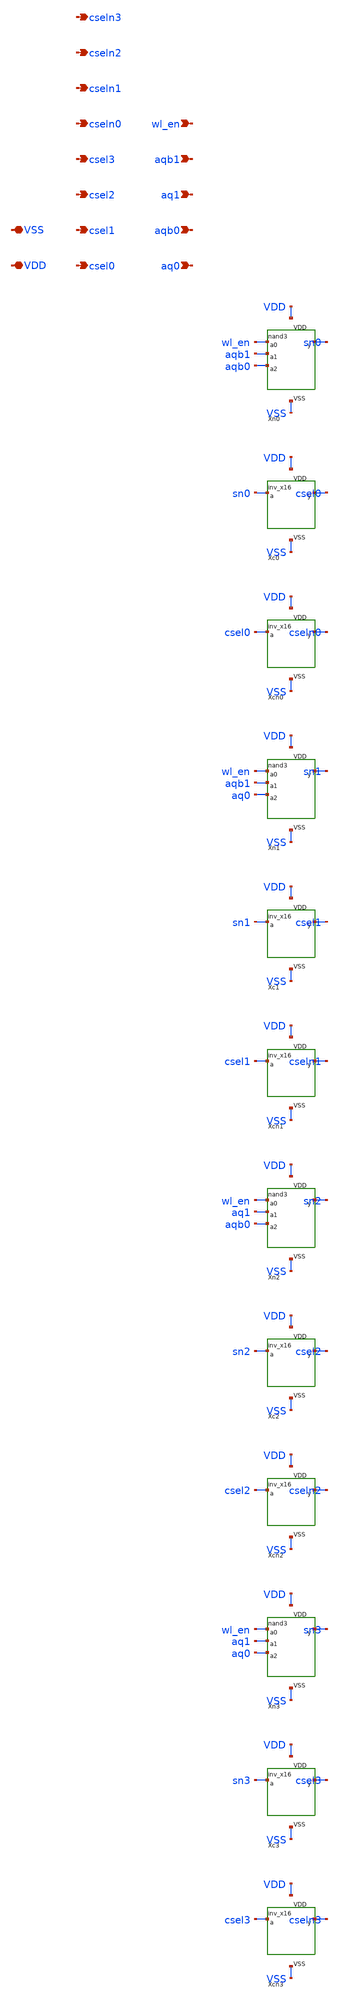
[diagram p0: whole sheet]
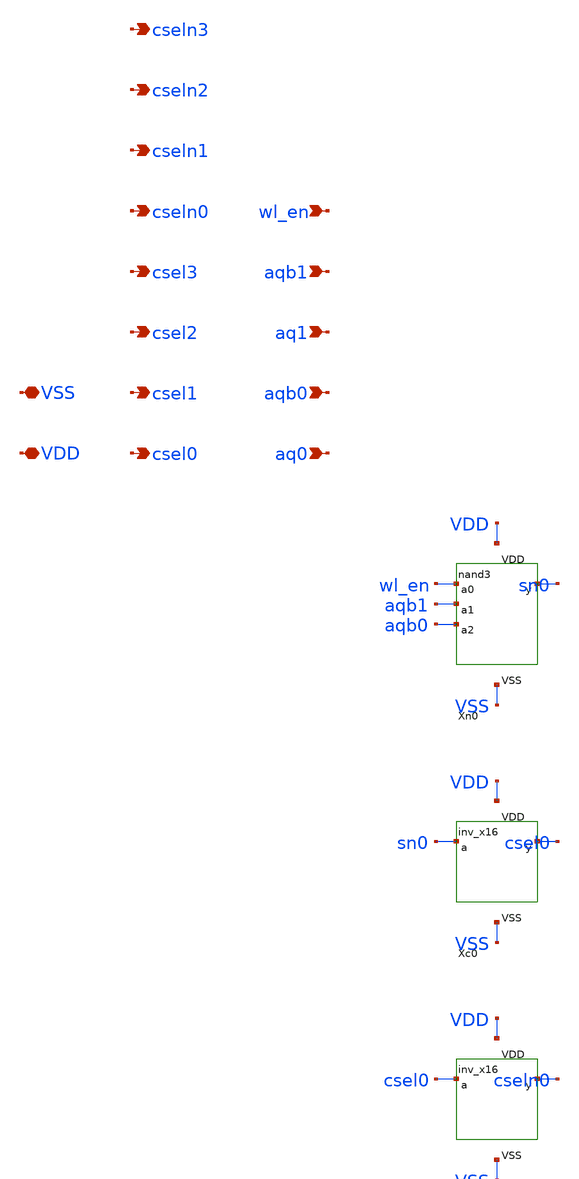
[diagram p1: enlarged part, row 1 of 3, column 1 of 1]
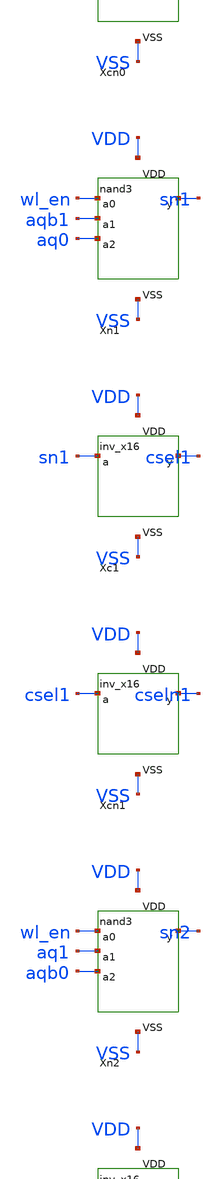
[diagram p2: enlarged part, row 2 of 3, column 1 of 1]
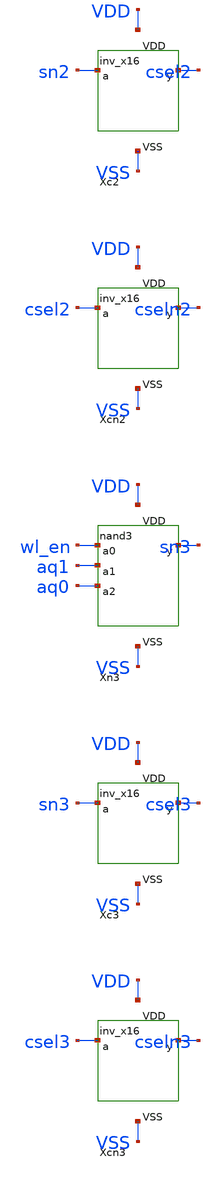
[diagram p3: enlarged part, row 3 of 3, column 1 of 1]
** sch_path: design/col_decode.sch
**.subckt col_decode aq0 aqb0 aq1 aqb1 wl_en csel0 csel1 csel2 csel3 cseln0 cseln1 cseln2 cseln3 VDD
*+ VSS
*.ipin aq0
*.ipin aqb0
*.ipin aq1
*.ipin aqb1
*.ipin wl_en
*.opin csel0
*.opin csel1
*.opin csel2
*.opin csel3
*.opin cseln0
*.opin cseln1
*.opin cseln2
*.opin cseln3
*.iopin VDD
*.iopin VSS
XXn0 wl_en aqb1 aqb0 sn0 VDD VSS nand3
XXc0 sn0 csel0 VDD VSS inv_x16
XXcn0 csel0 cseln0 VDD VSS inv_x16
XXn1 wl_en aqb1 aq0 sn1 VDD VSS nand3
XXc1 sn1 csel1 VDD VSS inv_x16
XXcn1 csel1 cseln1 VDD VSS inv_x16
XXn2 wl_en aq1 aqb0 sn2 VDD VSS nand3
XXc2 sn2 csel2 VDD VSS inv_x16
XXcn2 csel2 cseln2 VDD VSS inv_x16
XXn3 wl_en aq1 aq0 sn3 VDD VSS nand3
XXc3 sn3 csel3 VDD VSS inv_x16
XXcn3 csel3 cseln3 VDD VSS inv_x16
**.ends

* expanding   symbol:  nand3.sym # of pins=6
** sym_path: design/nand3.sym
** sch_path: design/nand3.sch
.subckt nand3 a0 a1 a2 y VDD VSS

*.ipin a0
*.ipin a1
*.ipin a2
*.opin y
*.iopin VDD
*.iopin VSS
XMP0 y a0 VDD VDD pfet_03v3 L=0.28u W=1u nf=1 ad='int((nf+1)/2) * W/nf * 0.18u' as='int((nf+2)/2) * W/nf * 0.18u'
+ pd='2*int((nf+1)/2) * (W/nf + 0.18u)' ps='2*int((nf+2)/2) * (W/nf + 0.18u)' nrd='0.18u / W' nrs='0.18u / W'
+ sa=0 sb=0 sd=0 m=1
XMP1 y a1 VDD VDD pfet_03v3 L=0.28u W=1u nf=1 ad='int((nf+1)/2) * W/nf * 0.18u' as='int((nf+2)/2) * W/nf * 0.18u'
+ pd='2*int((nf+1)/2) * (W/nf + 0.18u)' ps='2*int((nf+2)/2) * (W/nf + 0.18u)' nrd='0.18u / W' nrs='0.18u / W'
+ sa=0 sb=0 sd=0 m=1
XMP2 y a2 VDD VDD pfet_03v3 L=0.28u W=1u nf=1 ad='int((nf+1)/2) * W/nf * 0.18u' as='int((nf+2)/2) * W/nf * 0.18u'
+ pd='2*int((nf+1)/2) * (W/nf + 0.18u)' ps='2*int((nf+2)/2) * (W/nf + 0.18u)' nrd='0.18u / W' nrs='0.18u / W'
+ sa=0 sb=0 sd=0 m=1
XMN0 y a0 s1 VSS nfet_03v3 L=0.28u W=1.5u nf=1 ad='int((nf+1)/2) * W/nf * 0.18u' as='int((nf+2)/2) * W/nf * 0.18u'
+ pd='2*int((nf+1)/2) * (W/nf + 0.18u)' ps='2*int((nf+2)/2) * (W/nf + 0.18u)' nrd='0.18u / W' nrs='0.18u / W'
+ sa=0 sb=0 sd=0 m=1
XMN1 s1 a1 s2 VSS nfet_03v3 L=0.28u W=1.5u nf=1 ad='int((nf+1)/2) * W/nf * 0.18u' as='int((nf+2)/2) * W/nf * 0.18u'
+ pd='2*int((nf+1)/2) * (W/nf + 0.18u)' ps='2*int((nf+2)/2) * (W/nf + 0.18u)' nrd='0.18u / W' nrs='0.18u / W'
+ sa=0 sb=0 sd=0 m=1
XMN2 s2 a2 VSS VSS nfet_03v3 L=0.28u W=1.5u nf=1 ad='int((nf+1)/2) * W/nf * 0.18u' as='int((nf+2)/2) * W/nf * 0.18u'
+ pd='2*int((nf+1)/2) * (W/nf + 0.18u)' ps='2*int((nf+2)/2) * (W/nf + 0.18u)' nrd='0.18u / W' nrs='0.18u / W'
+ sa=0 sb=0 sd=0 m=1
.ends


* expanding   symbol:  inv_x16.sym # of pins=4
** sym_path: design/inv_x16.sym
** sch_path: design/inv_x16.sch
.subckt inv_x16 a y VDD VSS

*.ipin a
*.opin y
*.iopin VDD
*.iopin VSS
XMP y a VDD VDD pfet_03v3 L=0.28u W=16u nf=1 ad='int((nf+1)/2) * W/nf * 0.18u' as='int((nf+2)/2) * W/nf * 0.18u'
+ pd='2*int((nf+1)/2) * (W/nf + 0.18u)' ps='2*int((nf+2)/2) * (W/nf + 0.18u)' nrd='0.18u / W' nrs='0.18u / W'
+ sa=0 sb=0 sd=0 m=1
XMN y a VSS VSS nfet_03v3 L=0.28u W=8u nf=1 ad='int((nf+1)/2) * W/nf * 0.18u' as='int((nf+2)/2) * W/nf * 0.18u'
+ pd='2*int((nf+1)/2) * (W/nf + 0.18u)' ps='2*int((nf+2)/2) * (W/nf + 0.18u)' nrd='0.18u / W' nrs='0.18u / W'
+ sa=0 sb=0 sd=0 m=1
.ends

.end
